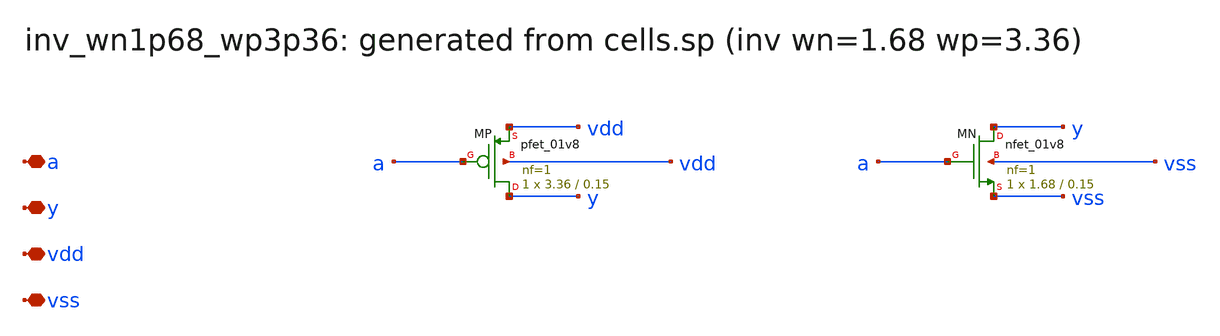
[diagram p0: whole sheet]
** sch_path: sram/xschem/inv_wn1p68_wp3p36.sch
**.subckt inv_wn1p68_wp3p36 a y vdd vss
*.iopin a
*.iopin y
*.iopin vdd
*.iopin vss
XMP y a vdd vdd sky130_fd_pr__pfet_01v8 L=0.15 W=3.36 nf=1 ad='int((nf+1)/2) * W/nf * 0.29' as='int((nf+2)/2) * W/nf * 0.29'
+ pd='2*int((nf+1)/2) * (W/nf + 0.29)' ps='2*int((nf+2)/2) * (W/nf + 0.29)' nrd='0.29 / W' nrs='0.29 / W'
+ sa=0 sb=0 sd=0 mult=1 m=1
XMN y a vss vss sky130_fd_pr__nfet_01v8 L=0.15 W=1.68 nf=1 ad='int((1 + 1)/2) * 1.68 / 1 * 0.29' as='int((1 + 2)/2) * 1.68 / 1 * 0.29'
+ pd='2*int((1 + 1)/2) * (1.68 / 1 + 0.29)' ps='2*int((1 + 2)/2) * (1.68 / 1 + 0.29)' nrd='0.29 / 1.68 '
+ nrs='0.29 / 1.68 ' sa=0 sb=0 sd=0 mult=1 m=1
**.ends
.end
